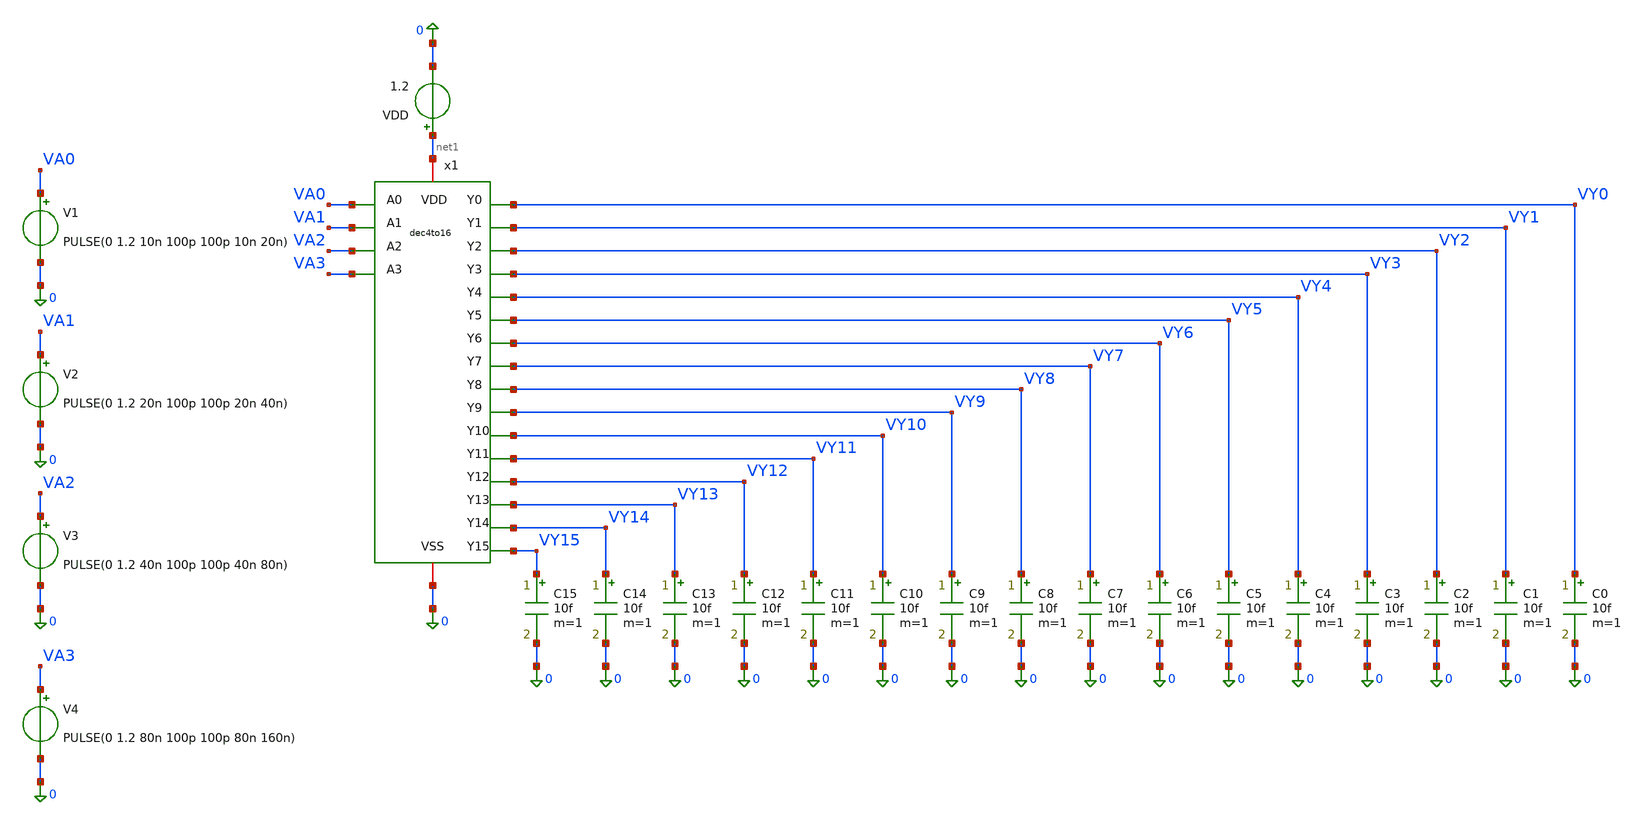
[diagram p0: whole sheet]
** sch_path: archives/dec4to16/tb_dec4to16.sch
**.subckt tb_dec4to16
x1 VA0 VA3 VY0 VY1 VY2 VY3 net1 0 VY4 VY5 VY6 VY7 VY8 VY9 VY10 VY11 VY12 VY13 VY14 VY15 VA1 VA2
+ dec4to16
V1 VA0 0 PULSE(0 1.2 10n 100p 100p 10n 20n)
V2 VA1 0 PULSE(0 1.2 20n 100p 100p 20n 40n)
V3 VA2 0 PULSE(0 1.2 40n 100p 100p 40n 80n)
V4 VA3 0 PULSE(0 1.2 80n 100p 100p 80n 160n)
VDD net1 0 1.2
C15 VY15 0 10f m=1
C14 VY14 0 10f m=1
C13 VY13 0 10f m=1
C12 VY12 0 10f m=1
C11 VY11 0 10f m=1
C10 VY10 0 10f m=1
C9 VY9 0 10f m=1
C8 VY8 0 10f m=1
C7 VY7 0 10f m=1
C0 VY0 0 10f m=1
C1 VY1 0 10f m=1
C2 VY2 0 10f m=1
C3 VY3 0 10f m=1
C4 VY4 0 10f m=1
C5 VY5 0 10f m=1
C6 VY6 0 10f m=1
**** begin user architecture code

.lib cornerMOSlv.lib mos_tt
.include /foss/pdks/ihp-sg13cmos5l/libs.ref/sg13cmos5l_stdcell/spice/sg13cmos5l_stdcell.spice


.control
  tran 100p 160n
  write tb_dec4to16.raw

  * ==========================================
  * AUTOMATED TRUTH TABLE VOLTAGE MEASUREMENTS
  * (Each state is sampled at its mid-window)
  * ==========================================
  meas tran v_y0_0000  find v(VY0)  at=5n
  meas tran v_y1_0001  find v(VY1)  at=15n
  meas tran v_y2_0010  find v(VY2)  at=25n
  meas tran v_y3_0011  find v(VY3)  at=35n
  meas tran v_y4_0100  find v(VY4)  at=45n
  meas tran v_y5_0101  find v(VY5)  at=55n
  meas tran v_y6_0110  find v(VY6)  at=65n
  meas tran v_y7_0111  find v(VY7)  at=75n
  meas tran v_y8_1000  find v(VY8)  at=85n
  meas tran v_y9_1001  find v(VY9)  at=95n
  meas tran v_y10_1010 find v(VY10) at=105n
  meas tran v_y11_1011 find v(VY11) at=115n
  meas tran v_y12_1100 find v(VY12) at=125n
  meas tran v_y13_1101 find v(VY13) at=135n
  meas tran v_y14_1110 find v(VY14) at=145n
  meas tran v_y15_1111 find v(VY15) at=155n

  * ==========================================
  * MULTI-TRACE OFFSET PLOTS
  * ==========================================
  * 1. 4-bit Binary Input Code (A0..A3)
  plot v(VA0) v(VA1)+1.5 v(VA2)+3.0 v(VA3)+4.5 title 'Decoder Inputs (A0, A1, A2, A3)' xlabel 'Time (s)'
+ ylabel 'Voltage (V)'

  * 2. Lower 8 Decoded Channels (Y0..Y7)
  plot v(VY0) v(VY1)+1.5 v(VY2)+3.0 v(VY3)+4.5 v(VY4)+6.0 v(VY5)+7.5 v(VY6)+9.0 v(VY7)+10.5 title 'Decoded Outputs (Y0..Y7)'
+ xlabel 'Time (s)' ylabel 'Voltage (V)'

  * 3. Upper 8 Decoded Channels (Y8..Y15)
  plot v(VY8) v(VY9)+1.5 v(VY10)+3.0 v(VY11)+4.5 v(VY12)+6.0 v(VY13)+7.5 v(VY14)+9.0 v(VY15)+10.5 title
+ 'Decoded Outputs (Y8..Y15)' xlabel 'Time (s)' ylabel 'Voltage (V)'
.endc


**** end user architecture code
**.ends
.end
